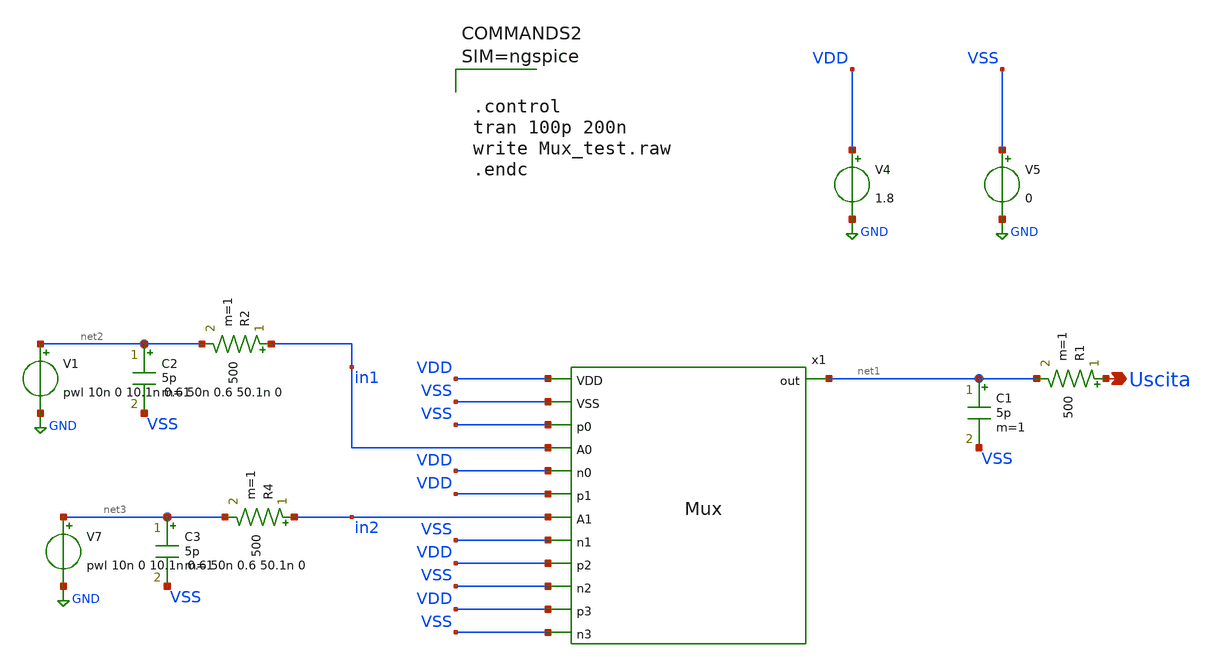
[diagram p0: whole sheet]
** sch_path: xschem/Mux_test.sch
**.subckt Mux_test Uscita
*.opin Uscita
V4 VDD GND 1.8
V5 VSS GND 0
V7 net3 GND pwl 10n 0 10.1n 0.6 50n 0.6 50.1n 0
C1 net1 VSS 5p m=1
R1 Uscita net1 500 m=1
C2 net2 VSS 5p m=1
R2 in1 net2 500 m=1
C3 net3 VSS 5p m=1
R4 in2 net3 500 m=1
x1 VDD VSS VSS in1 net1 VDD VDD in2 VSS VDD VSS VDD VSS Mux
V1 net2 GND pwl 10n 0 10.1n 0.6 50n 0.6 50.1n 0
**** begin user architecture code

** opencircuitdesign pdks install
.lib $::SKYWATER_MODELS/sky130.lib.spice tt





.control
tran 100p 200n
write Mux_test.raw
.endc



**** end user architecture code
**.ends

* expanding   symbol:  Mux.sym # of pins=13
** sym_path: xschem/Mux.sym
** sch_path: xschem/Mux.sch
.subckt Mux VDD VSS p0 A0 out n0 p1 A1 n1 p2 n2 p3 n3
*.ipin VDD
*.ipin VSS
*.ipin p0
*.ipin n0
*.ipin A0
*.ipin p1
*.ipin n1
*.ipin A1
*.ipin p2
*.ipin n2
*.ipin p3
*.ipin n3
*.opin out
R1 net1 VDD 800 m=1
XM8 out p0 A0 VDD sky130_fd_pr__pfet_01v8_lvt L=0.35 W=2 nf=2 ad='int((2 + 1)/2) * 2 / 2 * 0.29' as='int((2 + 2)/2) * 2 / 2 * 0.29'
+ pd='2*int((2 + 1)/2) * (2 / 2 + 0.29)' ps='2*int((2 + 2)/2) * (2 / 2 + 0.29)' nrd='0.29 / 2 ' nrs='0.29 / 2 '
+ sa=0 sb=0 sd=0 mult=1 m=1
XM9 A0 n0 out VSS sky130_fd_pr__nfet_01v8_lvt L=0.15 W=1 nf=1 ad='int((1 + 1)/2) * 1 / 1 * 0.29' as='int((1 + 2)/2) * 1 / 1 * 0.29'
+ pd='2*int((1 + 1)/2) * (1 / 1 + 0.29)' ps='2*int((1 + 2)/2) * (1 / 1 + 0.29)' nrd='0.29 / 1 ' nrs='0.29 / 1 '
+ sa=0 sb=0 sd=0 mult=1 m=1
XM10 out p1 A1 VDD sky130_fd_pr__pfet_01v8_lvt L=0.35 W=2 nf=2 ad='int((2 + 1)/2) * 2 / 2 * 0.29' as='int((2 + 2)/2) * 2 / 2 * 0.29'
+ pd='2*int((2 + 1)/2) * (2 / 2 + 0.29)' ps='2*int((2 + 2)/2) * (2 / 2 + 0.29)' nrd='0.29 / 2 ' nrs='0.29 / 2 '
+ sa=0 sb=0 sd=0 mult=1 m=1
XM1 A1 n1 out VSS sky130_fd_pr__nfet_01v8_lvt L=0.15 W=1 nf=1 ad='int((1 + 1)/2) * 1 / 1 * 0.29' as='int((1 + 2)/2) * 1 / 1 * 0.29'
+ pd='2*int((1 + 1)/2) * (1 / 1 + 0.29)' ps='2*int((1 + 2)/2) * (1 / 1 + 0.29)' nrd='0.29 / 1 ' nrs='0.29 / 1 '
+ sa=0 sb=0 sd=0 mult=1 m=1
XM2 out p2 net2 VDD sky130_fd_pr__pfet_01v8_lvt L=0.35 W=2 nf=2 ad='int((2 + 1)/2) * 2 / 2 * 0.29' as='int((2 + 2)/2) * 2 / 2 * 0.29'
+ pd='2*int((2 + 1)/2) * (2 / 2 + 0.29)' ps='2*int((2 + 2)/2) * (2 / 2 + 0.29)' nrd='0.29 / 2 ' nrs='0.29 / 2 '
+ sa=0 sb=0 sd=0 mult=1 m=1
XM3 net2 n2 out VSS sky130_fd_pr__nfet_01v8_lvt L=0.15 W=1 nf=1 ad='int((1 + 1)/2) * 1 / 1 * 0.29' as='int((1 + 2)/2) * 1 / 1 * 0.29'
+ pd='2*int((1 + 1)/2) * (1 / 1 + 0.29)' ps='2*int((1 + 2)/2) * (1 / 1 + 0.29)' nrd='0.29 / 1 ' nrs='0.29 / 1 '
+ sa=0 sb=0 sd=0 mult=1 m=1
XM4 out p3 net1 VDD sky130_fd_pr__pfet_01v8_lvt L=0.35 W=2 nf=2 ad='int((2 + 1)/2) * 2 / 2 * 0.29' as='int((2 + 2)/2) * 2 / 2 * 0.29'
+ pd='2*int((2 + 1)/2) * (2 / 2 + 0.29)' ps='2*int((2 + 2)/2) * (2 / 2 + 0.29)' nrd='0.29 / 2 ' nrs='0.29 / 2 '
+ sa=0 sb=0 sd=0 mult=1 m=1
XM5 net1 n3 out VSS sky130_fd_pr__nfet_01v8_lvt L=0.15 W=1 nf=1 ad='int((1 + 1)/2) * 1 / 1 * 0.29' as='int((1 + 2)/2) * 1 / 1 * 0.29'
+ pd='2*int((1 + 1)/2) * (1 / 1 + 0.29)' ps='2*int((1 + 2)/2) * (1 / 1 + 0.29)' nrd='0.29 / 1 ' nrs='0.29 / 1 '
+ sa=0 sb=0 sd=0 mult=1 m=1
R2 net2 VDD 400 m=1
R3 VSS net2 800 m=1
R4 VSS net1 400 m=1
.ends

.GLOBAL GND
.end
